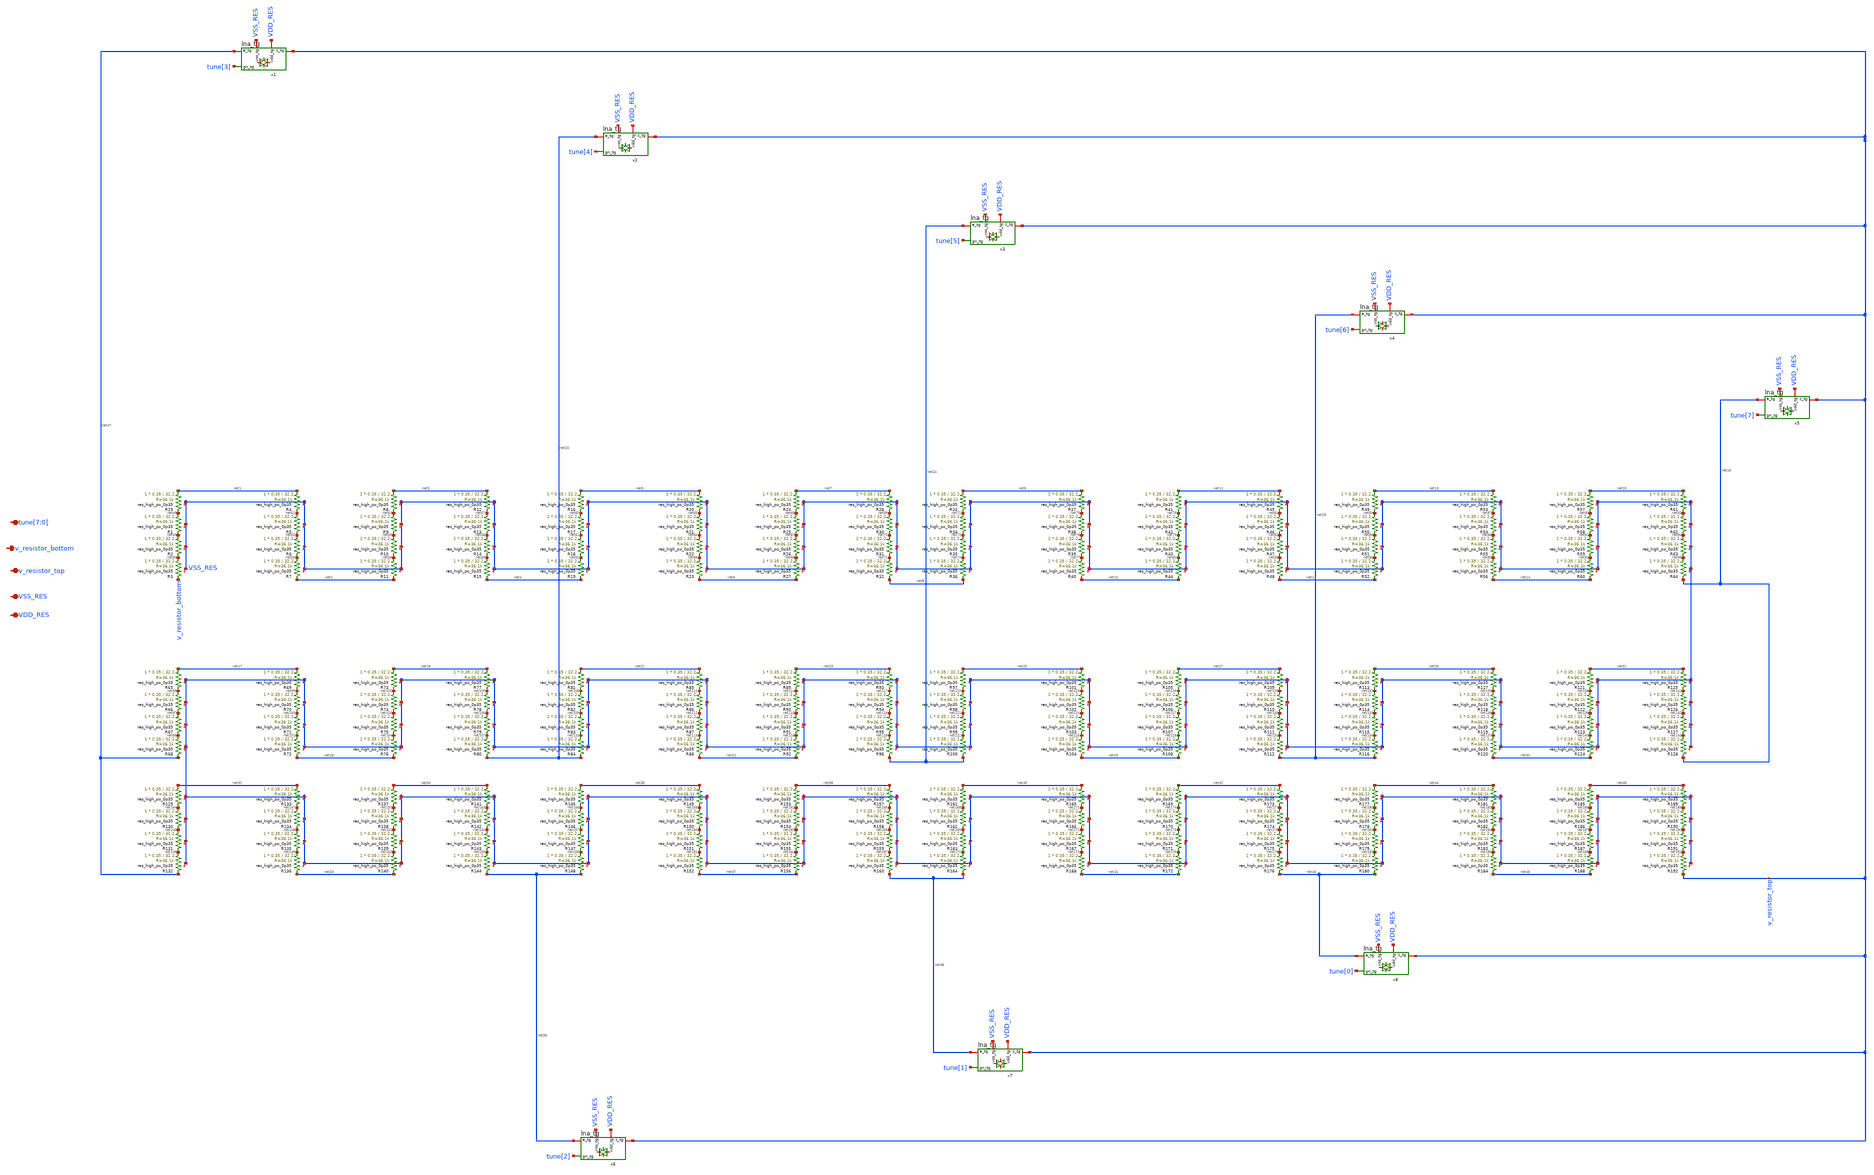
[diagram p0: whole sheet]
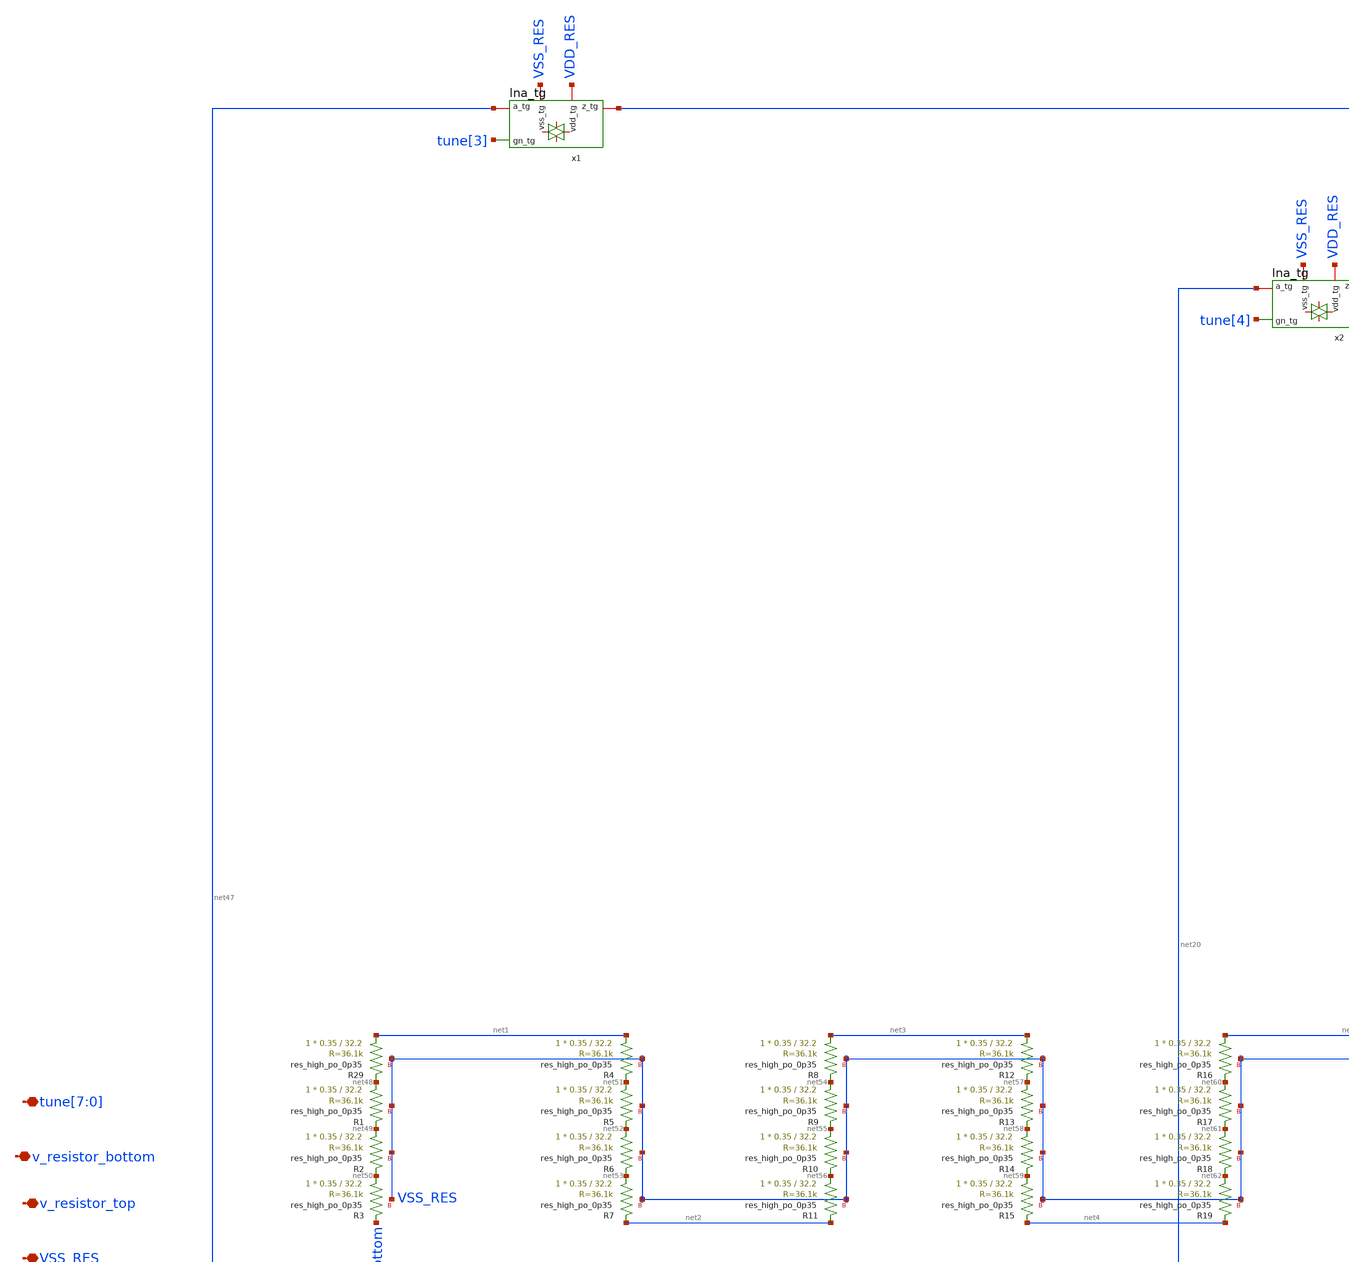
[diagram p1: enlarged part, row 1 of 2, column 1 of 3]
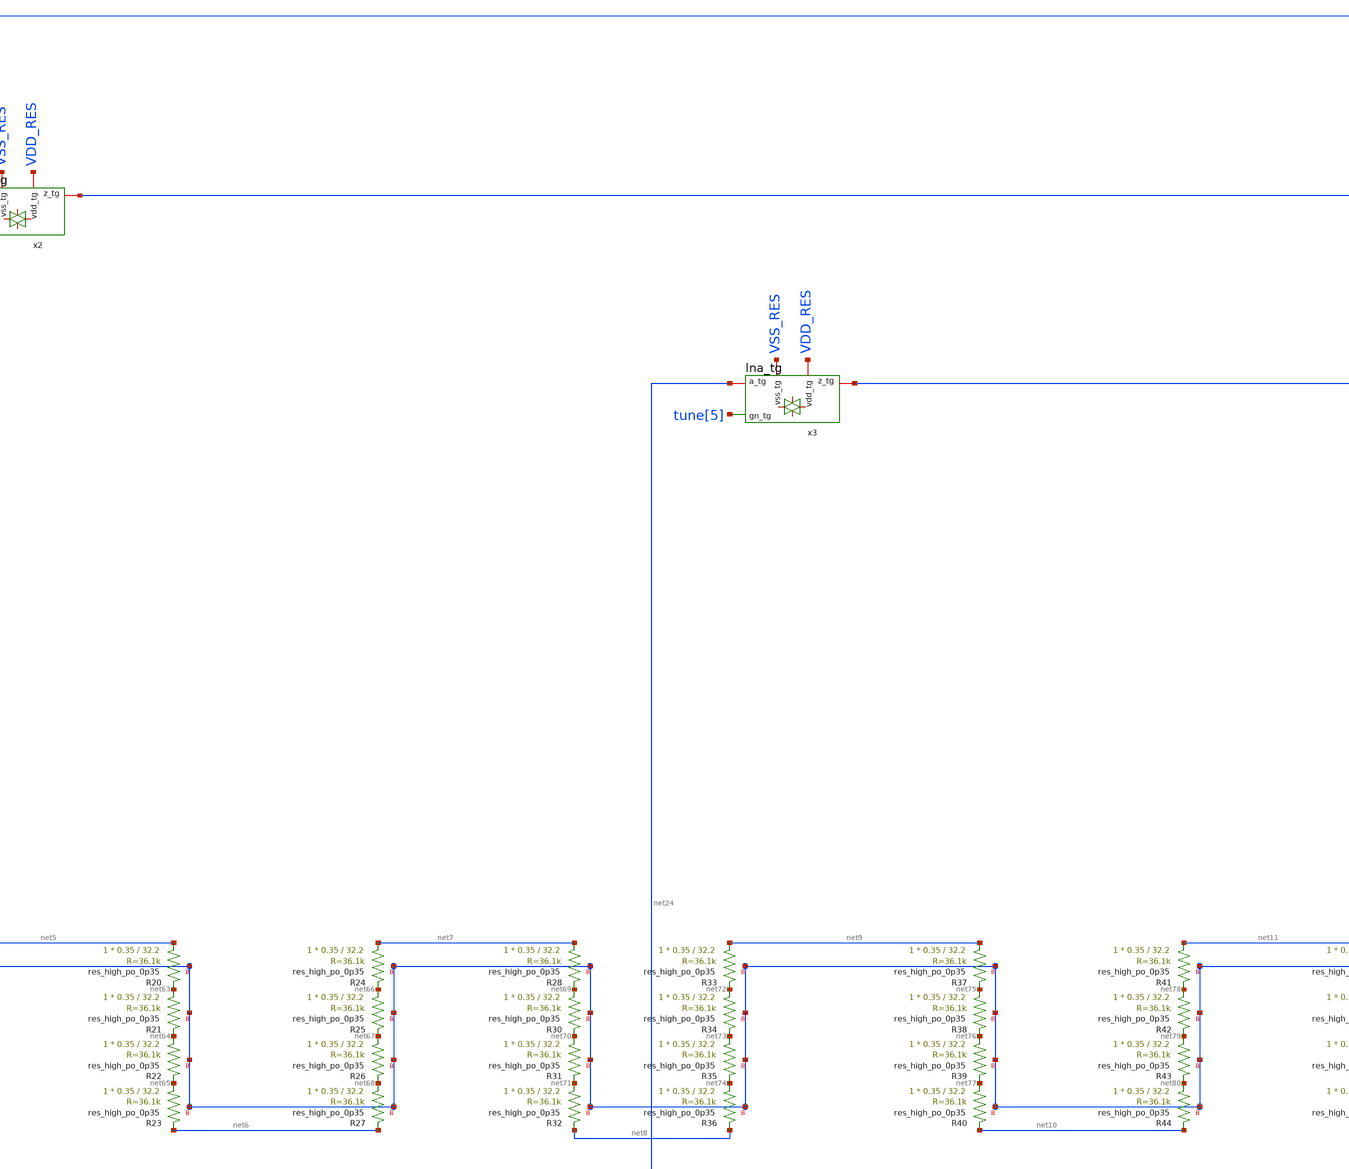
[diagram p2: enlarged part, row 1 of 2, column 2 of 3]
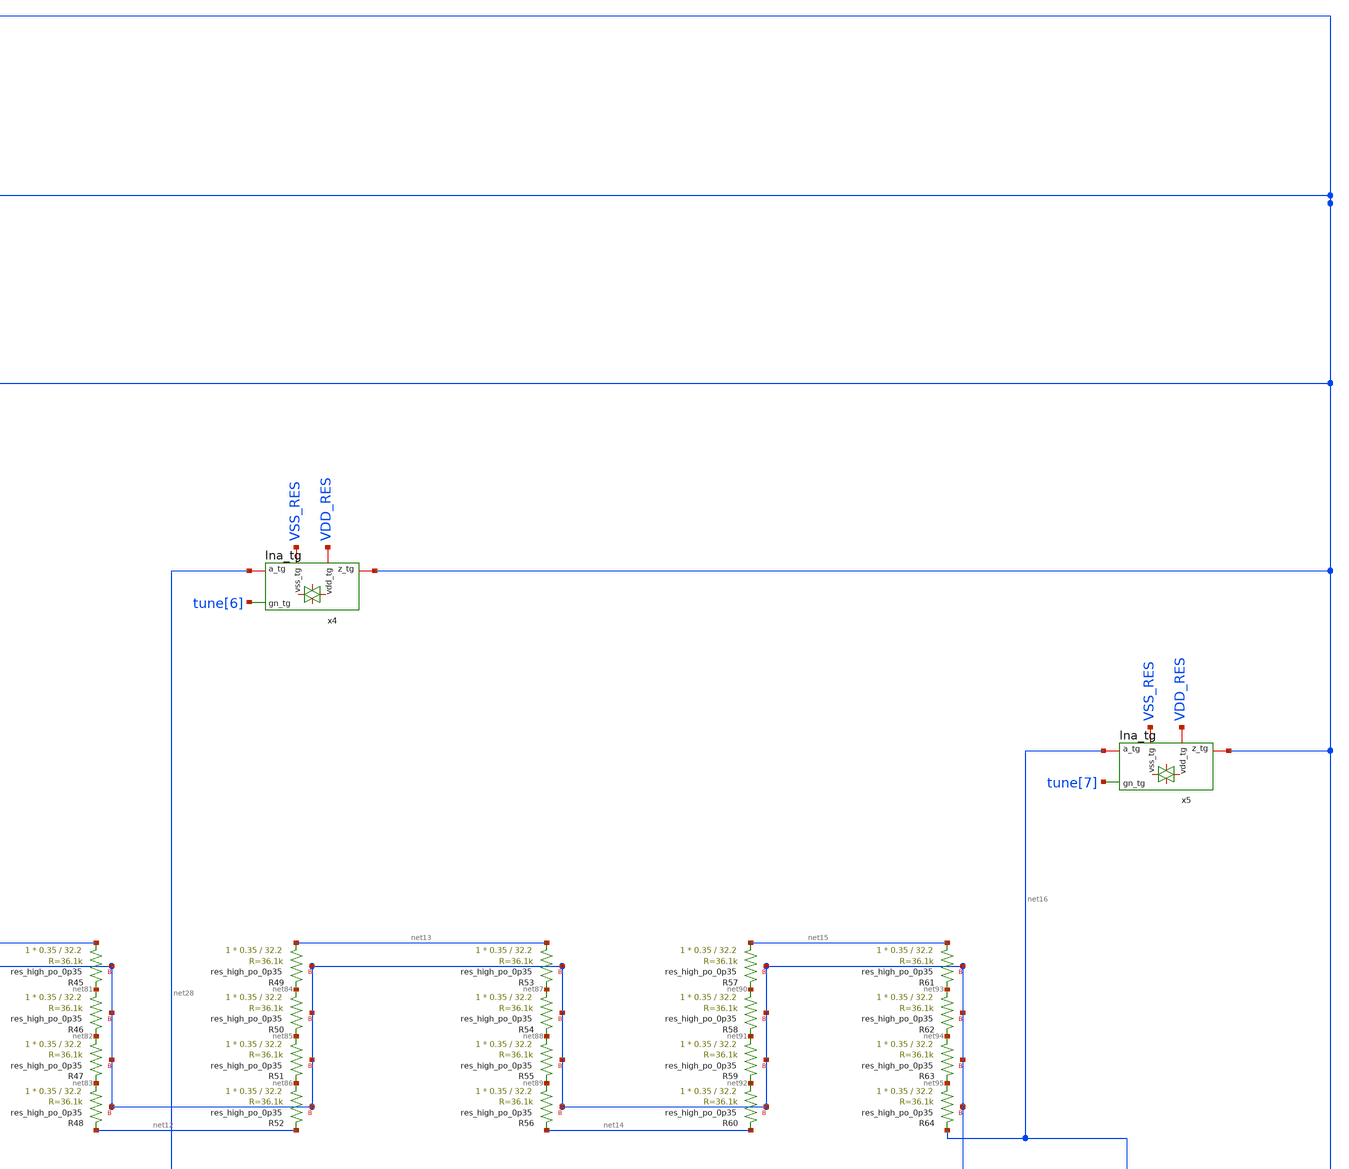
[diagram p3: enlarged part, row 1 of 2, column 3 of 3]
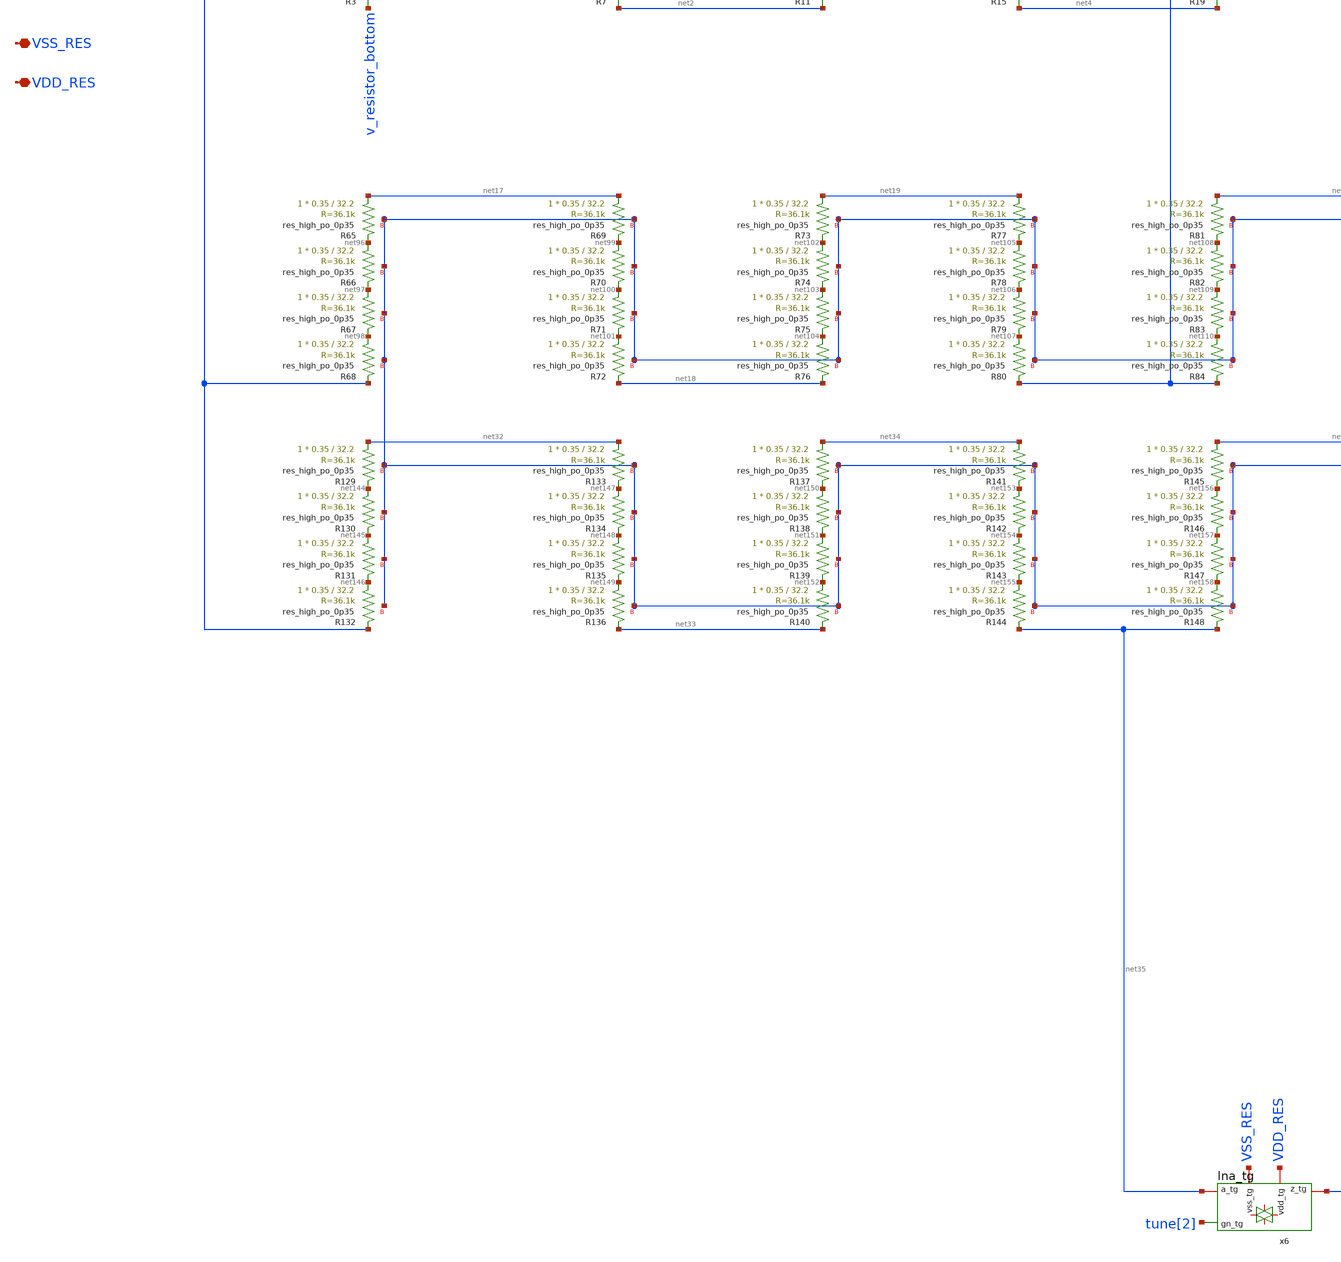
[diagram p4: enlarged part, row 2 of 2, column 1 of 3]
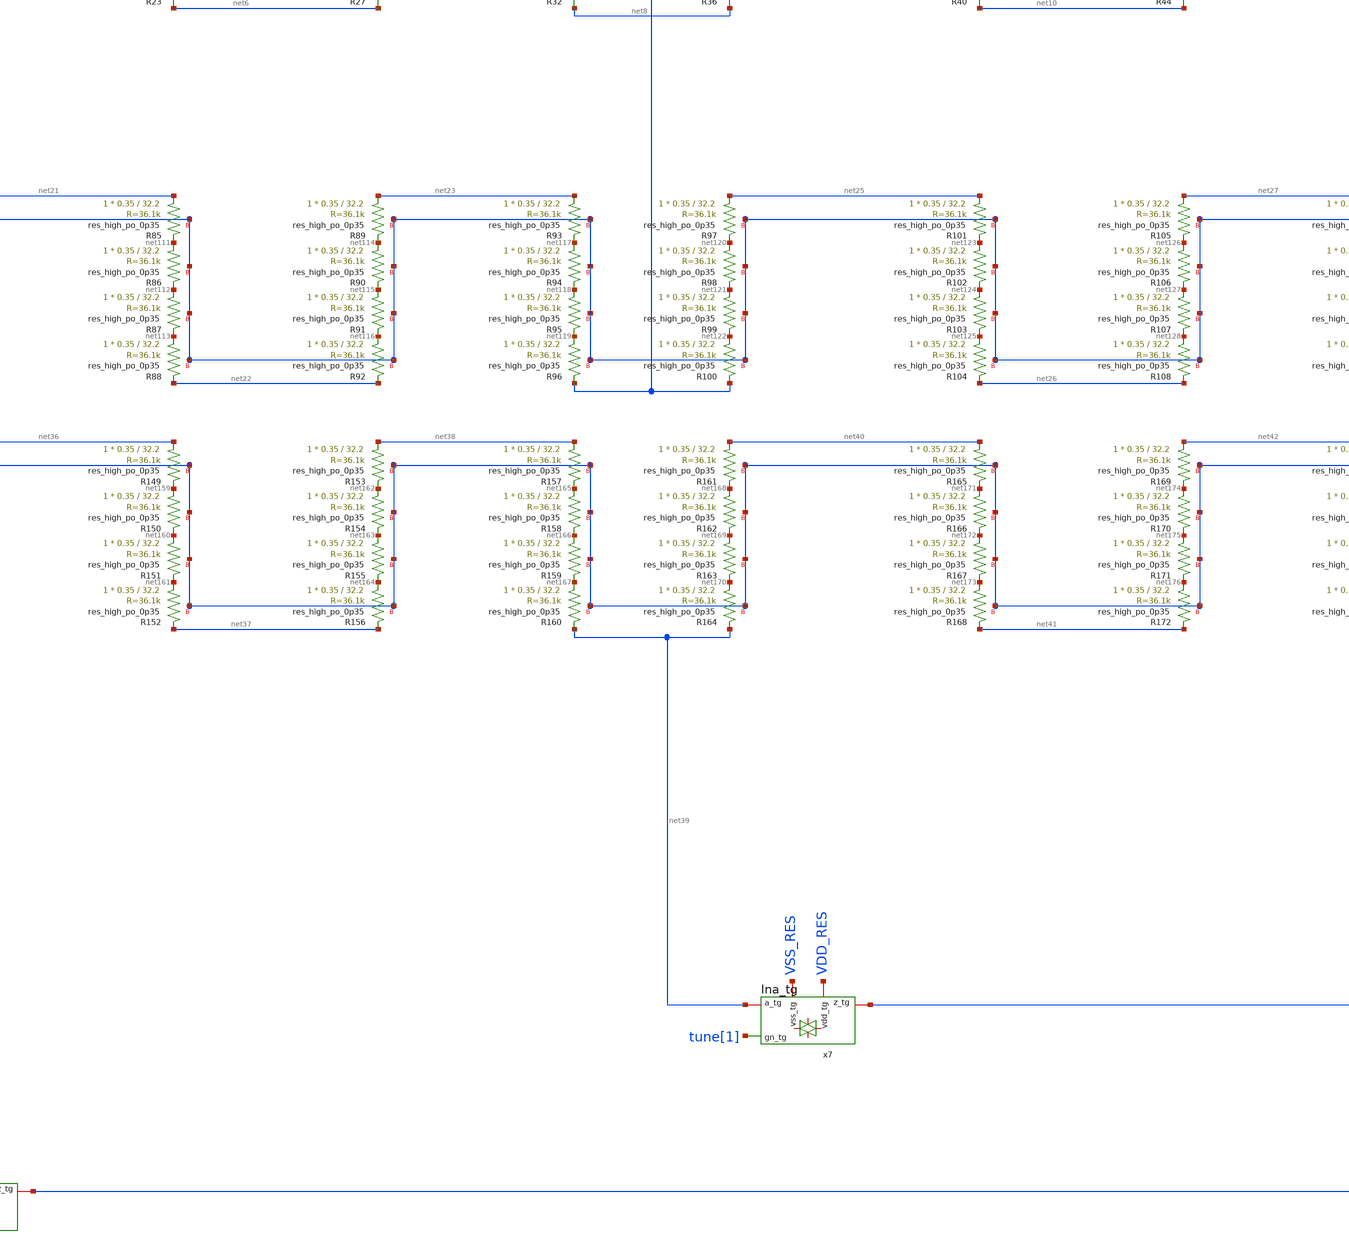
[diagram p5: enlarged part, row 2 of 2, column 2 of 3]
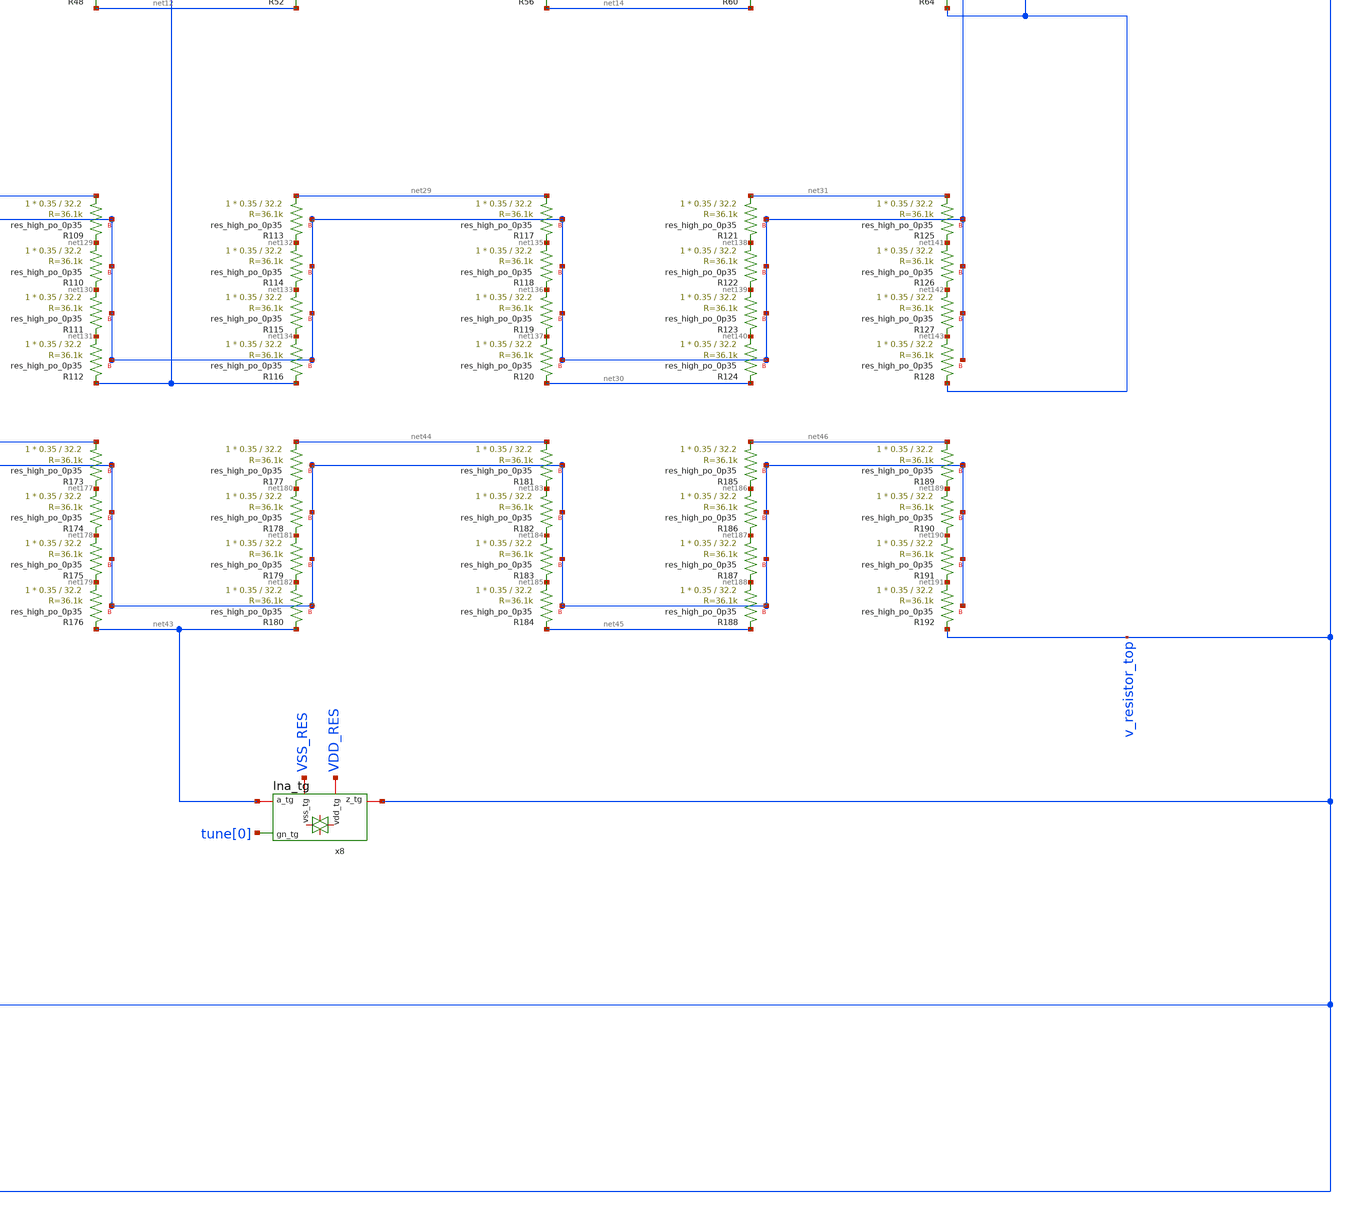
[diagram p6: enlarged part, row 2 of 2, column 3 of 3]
** sch_path: lna_bias_res.sch
**.subckt lna_bias_res v_resistor_bottom v_resistor_top VSS_RES VDD_RES
*+ tune[7],tune[6],tune[5],tune[4],tune[3],tune[2],tune[1],tune[0]
*.iopin v_resistor_bottom
*.iopin v_resistor_top
*.iopin VSS_RES
*.iopin VDD_RES
*.iopin tune[7],tune[6],tune[5],tune[4],tune[3],tune[2],tune[1],tune[0]
XR29 net1 net48 VSS_RES sky130_fd_pr__res_high_po_0p35 L=32.2 mult=1 m=1
XR1 net48 net49 VSS_RES sky130_fd_pr__res_high_po_0p35 L=32.2 mult=1 m=1
XR2 net49 net50 VSS_RES sky130_fd_pr__res_high_po_0p35 L=32.2 mult=1 m=1
XR3 net50 v_resistor_bottom VSS_RES sky130_fd_pr__res_high_po_0p35 L=32.2 mult=1 m=1
XR4 net1 net51 VSS_RES sky130_fd_pr__res_high_po_0p35 L=32.2 mult=1 m=1
XR5 net51 net52 VSS_RES sky130_fd_pr__res_high_po_0p35 L=32.2 mult=1 m=1
XR6 net52 net53 VSS_RES sky130_fd_pr__res_high_po_0p35 L=32.2 mult=1 m=1
XR7 net53 net2 VSS_RES sky130_fd_pr__res_high_po_0p35 L=32.2 mult=1 m=1
XR8 net3 net54 VSS_RES sky130_fd_pr__res_high_po_0p35 L=32.2 mult=1 m=1
XR9 net54 net55 VSS_RES sky130_fd_pr__res_high_po_0p35 L=32.2 mult=1 m=1
XR10 net55 net56 VSS_RES sky130_fd_pr__res_high_po_0p35 L=32.2 mult=1 m=1
XR11 net56 net2 VSS_RES sky130_fd_pr__res_high_po_0p35 L=32.2 mult=1 m=1
XR12 net3 net57 VSS_RES sky130_fd_pr__res_high_po_0p35 L=32.2 mult=1 m=1
XR13 net57 net58 VSS_RES sky130_fd_pr__res_high_po_0p35 L=32.2 mult=1 m=1
XR14 net58 net59 VSS_RES sky130_fd_pr__res_high_po_0p35 L=32.2 mult=1 m=1
XR15 net59 net4 VSS_RES sky130_fd_pr__res_high_po_0p35 L=32.2 mult=1 m=1
XR16 net5 net60 VSS_RES sky130_fd_pr__res_high_po_0p35 L=32.2 mult=1 m=1
XR17 net60 net61 VSS_RES sky130_fd_pr__res_high_po_0p35 L=32.2 mult=1 m=1
XR18 net61 net62 VSS_RES sky130_fd_pr__res_high_po_0p35 L=32.2 mult=1 m=1
XR19 net62 net4 VSS_RES sky130_fd_pr__res_high_po_0p35 L=32.2 mult=1 m=1
XR20 net5 net63 VSS_RES sky130_fd_pr__res_high_po_0p35 L=32.2 mult=1 m=1
XR21 net63 net64 VSS_RES sky130_fd_pr__res_high_po_0p35 L=32.2 mult=1 m=1
XR22 net64 net65 VSS_RES sky130_fd_pr__res_high_po_0p35 L=32.2 mult=1 m=1
XR23 net65 net6 VSS_RES sky130_fd_pr__res_high_po_0p35 L=32.2 mult=1 m=1
XR24 net7 net66 VSS_RES sky130_fd_pr__res_high_po_0p35 L=32.2 mult=1 m=1
XR25 net66 net67 VSS_RES sky130_fd_pr__res_high_po_0p35 L=32.2 mult=1 m=1
XR26 net67 net68 VSS_RES sky130_fd_pr__res_high_po_0p35 L=32.2 mult=1 m=1
XR27 net68 net6 VSS_RES sky130_fd_pr__res_high_po_0p35 L=32.2 mult=1 m=1
XR28 net7 net69 VSS_RES sky130_fd_pr__res_high_po_0p35 L=32.2 mult=1 m=1
XR30 net69 net70 VSS_RES sky130_fd_pr__res_high_po_0p35 L=32.2 mult=1 m=1
XR31 net70 net71 VSS_RES sky130_fd_pr__res_high_po_0p35 L=32.2 mult=1 m=1
XR32 net71 net8 VSS_RES sky130_fd_pr__res_high_po_0p35 L=32.2 mult=1 m=1
XR33 net9 net72 VSS_RES sky130_fd_pr__res_high_po_0p35 L=32.2 mult=1 m=1
XR34 net72 net73 VSS_RES sky130_fd_pr__res_high_po_0p35 L=32.2 mult=1 m=1
XR35 net73 net74 VSS_RES sky130_fd_pr__res_high_po_0p35 L=32.2 mult=1 m=1
XR36 net74 net8 VSS_RES sky130_fd_pr__res_high_po_0p35 L=32.2 mult=1 m=1
XR37 net9 net75 VSS_RES sky130_fd_pr__res_high_po_0p35 L=32.2 mult=1 m=1
XR38 net75 net76 VSS_RES sky130_fd_pr__res_high_po_0p35 L=32.2 mult=1 m=1
XR39 net76 net77 VSS_RES sky130_fd_pr__res_high_po_0p35 L=32.2 mult=1 m=1
XR40 net77 net10 VSS_RES sky130_fd_pr__res_high_po_0p35 L=32.2 mult=1 m=1
XR41 net11 net78 VSS_RES sky130_fd_pr__res_high_po_0p35 L=32.2 mult=1 m=1
XR42 net78 net79 VSS_RES sky130_fd_pr__res_high_po_0p35 L=32.2 mult=1 m=1
XR43 net79 net80 VSS_RES sky130_fd_pr__res_high_po_0p35 L=32.2 mult=1 m=1
XR44 net80 net10 VSS_RES sky130_fd_pr__res_high_po_0p35 L=32.2 mult=1 m=1
XR45 net11 net81 VSS_RES sky130_fd_pr__res_high_po_0p35 L=32.2 mult=1 m=1
XR46 net81 net82 VSS_RES sky130_fd_pr__res_high_po_0p35 L=32.2 mult=1 m=1
XR47 net82 net83 VSS_RES sky130_fd_pr__res_high_po_0p35 L=32.2 mult=1 m=1
XR48 net83 net12 VSS_RES sky130_fd_pr__res_high_po_0p35 L=32.2 mult=1 m=1
XR49 net13 net84 VSS_RES sky130_fd_pr__res_high_po_0p35 L=32.2 mult=1 m=1
XR50 net84 net85 VSS_RES sky130_fd_pr__res_high_po_0p35 L=32.2 mult=1 m=1
XR51 net85 net86 VSS_RES sky130_fd_pr__res_high_po_0p35 L=32.2 mult=1 m=1
XR52 net86 net12 VSS_RES sky130_fd_pr__res_high_po_0p35 L=32.2 mult=1 m=1
XR53 net13 net87 VSS_RES sky130_fd_pr__res_high_po_0p35 L=32.2 mult=1 m=1
XR54 net87 net88 VSS_RES sky130_fd_pr__res_high_po_0p35 L=32.2 mult=1 m=1
XR55 net88 net89 VSS_RES sky130_fd_pr__res_high_po_0p35 L=32.2 mult=1 m=1
XR56 net89 net14 VSS_RES sky130_fd_pr__res_high_po_0p35 L=32.2 mult=1 m=1
XR57 net15 net90 VSS_RES sky130_fd_pr__res_high_po_0p35 L=32.2 mult=1 m=1
XR58 net90 net91 VSS_RES sky130_fd_pr__res_high_po_0p35 L=32.2 mult=1 m=1
XR59 net91 net92 VSS_RES sky130_fd_pr__res_high_po_0p35 L=32.2 mult=1 m=1
XR60 net92 net14 VSS_RES sky130_fd_pr__res_high_po_0p35 L=32.2 mult=1 m=1
XR61 net15 net93 VSS_RES sky130_fd_pr__res_high_po_0p35 L=32.2 mult=1 m=1
XR62 net93 net94 VSS_RES sky130_fd_pr__res_high_po_0p35 L=32.2 mult=1 m=1
XR63 net94 net95 VSS_RES sky130_fd_pr__res_high_po_0p35 L=32.2 mult=1 m=1
XR64 net95 net16 VSS_RES sky130_fd_pr__res_high_po_0p35 L=32.2 mult=1 m=1
XR65 net17 net96 VSS_RES sky130_fd_pr__res_high_po_0p35 L=32.2 mult=1 m=1
XR66 net96 net97 VSS_RES sky130_fd_pr__res_high_po_0p35 L=32.2 mult=1 m=1
XR67 net97 net98 VSS_RES sky130_fd_pr__res_high_po_0p35 L=32.2 mult=1 m=1
XR68 net98 net47 VSS_RES sky130_fd_pr__res_high_po_0p35 L=32.2 mult=1 m=1
XR69 net17 net99 VSS_RES sky130_fd_pr__res_high_po_0p35 L=32.2 mult=1 m=1
XR70 net99 net100 VSS_RES sky130_fd_pr__res_high_po_0p35 L=32.2 mult=1 m=1
XR71 net100 net101 VSS_RES sky130_fd_pr__res_high_po_0p35 L=32.2 mult=1 m=1
XR72 net101 net18 VSS_RES sky130_fd_pr__res_high_po_0p35 L=32.2 mult=1 m=1
XR73 net19 net102 VSS_RES sky130_fd_pr__res_high_po_0p35 L=32.2 mult=1 m=1
XR74 net102 net103 VSS_RES sky130_fd_pr__res_high_po_0p35 L=32.2 mult=1 m=1
XR75 net103 net104 VSS_RES sky130_fd_pr__res_high_po_0p35 L=32.2 mult=1 m=1
XR76 net104 net18 VSS_RES sky130_fd_pr__res_high_po_0p35 L=32.2 mult=1 m=1
XR77 net19 net105 VSS_RES sky130_fd_pr__res_high_po_0p35 L=32.2 mult=1 m=1
XR78 net105 net106 VSS_RES sky130_fd_pr__res_high_po_0p35 L=32.2 mult=1 m=1
XR79 net106 net107 VSS_RES sky130_fd_pr__res_high_po_0p35 L=32.2 mult=1 m=1
XR80 net107 net20 VSS_RES sky130_fd_pr__res_high_po_0p35 L=32.2 mult=1 m=1
XR81 net21 net108 VSS_RES sky130_fd_pr__res_high_po_0p35 L=32.2 mult=1 m=1
XR82 net108 net109 VSS_RES sky130_fd_pr__res_high_po_0p35 L=32.2 mult=1 m=1
XR83 net109 net110 VSS_RES sky130_fd_pr__res_high_po_0p35 L=32.2 mult=1 m=1
XR84 net110 net20 VSS_RES sky130_fd_pr__res_high_po_0p35 L=32.2 mult=1 m=1
XR85 net21 net111 VSS_RES sky130_fd_pr__res_high_po_0p35 L=32.2 mult=1 m=1
XR86 net111 net112 VSS_RES sky130_fd_pr__res_high_po_0p35 L=32.2 mult=1 m=1
XR87 net112 net113 VSS_RES sky130_fd_pr__res_high_po_0p35 L=32.2 mult=1 m=1
XR88 net113 net22 VSS_RES sky130_fd_pr__res_high_po_0p35 L=32.2 mult=1 m=1
XR89 net23 net114 VSS_RES sky130_fd_pr__res_high_po_0p35 L=32.2 mult=1 m=1
XR90 net114 net115 VSS_RES sky130_fd_pr__res_high_po_0p35 L=32.2 mult=1 m=1
XR91 net115 net116 VSS_RES sky130_fd_pr__res_high_po_0p35 L=32.2 mult=1 m=1
XR92 net116 net22 VSS_RES sky130_fd_pr__res_high_po_0p35 L=32.2 mult=1 m=1
XR93 net23 net117 VSS_RES sky130_fd_pr__res_high_po_0p35 L=32.2 mult=1 m=1
XR94 net117 net118 VSS_RES sky130_fd_pr__res_high_po_0p35 L=32.2 mult=1 m=1
XR95 net118 net119 VSS_RES sky130_fd_pr__res_high_po_0p35 L=32.2 mult=1 m=1
XR96 net119 net24 VSS_RES sky130_fd_pr__res_high_po_0p35 L=32.2 mult=1 m=1
XR97 net25 net120 VSS_RES sky130_fd_pr__res_high_po_0p35 L=32.2 mult=1 m=1
XR98 net120 net121 VSS_RES sky130_fd_pr__res_high_po_0p35 L=32.2 mult=1 m=1
XR99 net121 net122 VSS_RES sky130_fd_pr__res_high_po_0p35 L=32.2 mult=1 m=1
XR100 net122 net24 VSS_RES sky130_fd_pr__res_high_po_0p35 L=32.2 mult=1 m=1
XR101 net25 net123 VSS_RES sky130_fd_pr__res_high_po_0p35 L=32.2 mult=1 m=1
XR102 net123 net124 VSS_RES sky130_fd_pr__res_high_po_0p35 L=32.2 mult=1 m=1
XR103 net124 net125 VSS_RES sky130_fd_pr__res_high_po_0p35 L=32.2 mult=1 m=1
XR104 net125 net26 VSS_RES sky130_fd_pr__res_high_po_0p35 L=32.2 mult=1 m=1
XR105 net27 net126 VSS_RES sky130_fd_pr__res_high_po_0p35 L=32.2 mult=1 m=1
XR106 net126 net127 VSS_RES sky130_fd_pr__res_high_po_0p35 L=32.2 mult=1 m=1
XR107 net127 net128 VSS_RES sky130_fd_pr__res_high_po_0p35 L=32.2 mult=1 m=1
XR108 net128 net26 VSS_RES sky130_fd_pr__res_high_po_0p35 L=32.2 mult=1 m=1
XR109 net27 net129 VSS_RES sky130_fd_pr__res_high_po_0p35 L=32.2 mult=1 m=1
XR110 net129 net130 VSS_RES sky130_fd_pr__res_high_po_0p35 L=32.2 mult=1 m=1
XR111 net130 net131 VSS_RES sky130_fd_pr__res_high_po_0p35 L=32.2 mult=1 m=1
XR112 net131 net28 VSS_RES sky130_fd_pr__res_high_po_0p35 L=32.2 mult=1 m=1
XR113 net29 net132 VSS_RES sky130_fd_pr__res_high_po_0p35 L=32.2 mult=1 m=1
XR114 net132 net133 VSS_RES sky130_fd_pr__res_high_po_0p35 L=32.2 mult=1 m=1
XR115 net133 net134 VSS_RES sky130_fd_pr__res_high_po_0p35 L=32.2 mult=1 m=1
XR116 net134 net28 VSS_RES sky130_fd_pr__res_high_po_0p35 L=32.2 mult=1 m=1
XR117 net29 net135 VSS_RES sky130_fd_pr__res_high_po_0p35 L=32.2 mult=1 m=1
XR118 net135 net136 VSS_RES sky130_fd_pr__res_high_po_0p35 L=32.2 mult=1 m=1
XR119 net136 net137 VSS_RES sky130_fd_pr__res_high_po_0p35 L=32.2 mult=1 m=1
XR120 net137 net30 VSS_RES sky130_fd_pr__res_high_po_0p35 L=32.2 mult=1 m=1
XR121 net31 net138 VSS_RES sky130_fd_pr__res_high_po_0p35 L=32.2 mult=1 m=1
XR122 net138 net139 VSS_RES sky130_fd_pr__res_high_po_0p35 L=32.2 mult=1 m=1
XR123 net139 net140 VSS_RES sky130_fd_pr__res_high_po_0p35 L=32.2 mult=1 m=1
XR124 net140 net30 VSS_RES sky130_fd_pr__res_high_po_0p35 L=32.2 mult=1 m=1
XR125 net31 net141 VSS_RES sky130_fd_pr__res_high_po_0p35 L=32.2 mult=1 m=1
XR126 net141 net142 VSS_RES sky130_fd_pr__res_high_po_0p35 L=32.2 mult=1 m=1
XR127 net142 net143 VSS_RES sky130_fd_pr__res_high_po_0p35 L=32.2 mult=1 m=1
XR128 net143 net16 VSS_RES sky130_fd_pr__res_high_po_0p35 L=32.2 mult=1 m=1
XR129 net32 net144 VSS_RES sky130_fd_pr__res_high_po_0p35 L=32.2 mult=1 m=1
XR130 net144 net145 VSS_RES sky130_fd_pr__res_high_po_0p35 L=32.2 mult=1 m=1
XR131 net145 net146 VSS_RES sky130_fd_pr__res_high_po_0p35 L=32.2 mult=1 m=1
XR132 net146 net47 VSS_RES sky130_fd_pr__res_high_po_0p35 L=32.2 mult=1 m=1
XR133 net32 net147 VSS_RES sky130_fd_pr__res_high_po_0p35 L=32.2 mult=1 m=1
XR134 net147 net148 VSS_RES sky130_fd_pr__res_high_po_0p35 L=32.2 mult=1 m=1
XR135 net148 net149 VSS_RES sky130_fd_pr__res_high_po_0p35 L=32.2 mult=1 m=1
XR136 net149 net33 VSS_RES sky130_fd_pr__res_high_po_0p35 L=32.2 mult=1 m=1
XR137 net34 net150 VSS_RES sky130_fd_pr__res_high_po_0p35 L=32.2 mult=1 m=1
XR138 net150 net151 VSS_RES sky130_fd_pr__res_high_po_0p35 L=32.2 mult=1 m=1
XR139 net151 net152 VSS_RES sky130_fd_pr__res_high_po_0p35 L=32.2 mult=1 m=1
XR140 net152 net33 VSS_RES sky130_fd_pr__res_high_po_0p35 L=32.2 mult=1 m=1
XR141 net34 net153 VSS_RES sky130_fd_pr__res_high_po_0p35 L=32.2 mult=1 m=1
XR142 net153 net154 VSS_RES sky130_fd_pr__res_high_po_0p35 L=32.2 mult=1 m=1
XR143 net154 net155 VSS_RES sky130_fd_pr__res_high_po_0p35 L=32.2 mult=1 m=1
XR144 net155 net35 VSS_RES sky130_fd_pr__res_high_po_0p35 L=32.2 mult=1 m=1
XR145 net36 net156 VSS_RES sky130_fd_pr__res_high_po_0p35 L=32.2 mult=1 m=1
XR146 net156 net157 VSS_RES sky130_fd_pr__res_high_po_0p35 L=32.2 mult=1 m=1
XR147 net157 net158 VSS_RES sky130_fd_pr__res_high_po_0p35 L=32.2 mult=1 m=1
XR148 net158 net35 VSS_RES sky130_fd_pr__res_high_po_0p35 L=32.2 mult=1 m=1
XR149 net36 net159 VSS_RES sky130_fd_pr__res_high_po_0p35 L=32.2 mult=1 m=1
XR150 net159 net160 VSS_RES sky130_fd_pr__res_high_po_0p35 L=32.2 mult=1 m=1
XR151 net160 net161 VSS_RES sky130_fd_pr__res_high_po_0p35 L=32.2 mult=1 m=1
XR152 net161 net37 VSS_RES sky130_fd_pr__res_high_po_0p35 L=32.2 mult=1 m=1
XR153 net38 net162 VSS_RES sky130_fd_pr__res_high_po_0p35 L=32.2 mult=1 m=1
XR154 net162 net163 VSS_RES sky130_fd_pr__res_high_po_0p35 L=32.2 mult=1 m=1
XR155 net163 net164 VSS_RES sky130_fd_pr__res_high_po_0p35 L=32.2 mult=1 m=1
XR156 net164 net37 VSS_RES sky130_fd_pr__res_high_po_0p35 L=32.2 mult=1 m=1
XR157 net38 net165 VSS_RES sky130_fd_pr__res_high_po_0p35 L=32.2 mult=1 m=1
XR158 net165 net166 VSS_RES sky130_fd_pr__res_high_po_0p35 L=32.2 mult=1 m=1
XR159 net166 net167 VSS_RES sky130_fd_pr__res_high_po_0p35 L=32.2 mult=1 m=1
XR160 net167 net39 VSS_RES sky130_fd_pr__res_high_po_0p35 L=32.2 mult=1 m=1
XR161 net40 net168 VSS_RES sky130_fd_pr__res_high_po_0p35 L=32.2 mult=1 m=1
XR162 net168 net169 VSS_RES sky130_fd_pr__res_high_po_0p35 L=32.2 mult=1 m=1
XR163 net169 net170 VSS_RES sky130_fd_pr__res_high_po_0p35 L=32.2 mult=1 m=1
XR164 net170 net39 VSS_RES sky130_fd_pr__res_high_po_0p35 L=32.2 mult=1 m=1
XR165 net40 net171 VSS_RES sky130_fd_pr__res_high_po_0p35 L=32.2 mult=1 m=1
XR166 net171 net172 VSS_RES sky130_fd_pr__res_high_po_0p35 L=32.2 mult=1 m=1
XR167 net172 net173 VSS_RES sky130_fd_pr__res_high_po_0p35 L=32.2 mult=1 m=1
XR168 net173 net41 VSS_RES sky130_fd_pr__res_high_po_0p35 L=32.2 mult=1 m=1
XR169 net42 net174 VSS_RES sky130_fd_pr__res_high_po_0p35 L=32.2 mult=1 m=1
XR170 net174 net175 VSS_RES sky130_fd_pr__res_high_po_0p35 L=32.2 mult=1 m=1
XR171 net175 net176 VSS_RES sky130_fd_pr__res_high_po_0p35 L=32.2 mult=1 m=1
XR172 net176 net41 VSS_RES sky130_fd_pr__res_high_po_0p35 L=32.2 mult=1 m=1
XR173 net42 net177 VSS_RES sky130_fd_pr__res_high_po_0p35 L=32.2 mult=1 m=1
XR174 net177 net178 VSS_RES sky130_fd_pr__res_high_po_0p35 L=32.2 mult=1 m=1
XR175 net178 net179 VSS_RES sky130_fd_pr__res_high_po_0p35 L=32.2 mult=1 m=1
XR176 net179 net43 VSS_RES sky130_fd_pr__res_high_po_0p35 L=32.2 mult=1 m=1
XR177 net44 net180 VSS_RES sky130_fd_pr__res_high_po_0p35 L=32.2 mult=1 m=1
XR178 net180 net181 VSS_RES sky130_fd_pr__res_high_po_0p35 L=32.2 mult=1 m=1
XR179 net181 net182 VSS_RES sky130_fd_pr__res_high_po_0p35 L=32.2 mult=1 m=1
XR180 net182 net43 VSS_RES sky130_fd_pr__res_high_po_0p35 L=32.2 mult=1 m=1
XR181 net44 net183 VSS_RES sky130_fd_pr__res_high_po_0p35 L=32.2 mult=1 m=1
XR182 net183 net184 VSS_RES sky130_fd_pr__res_high_po_0p35 L=32.2 mult=1 m=1
XR183 net184 net185 VSS_RES sky130_fd_pr__res_high_po_0p35 L=32.2 mult=1 m=1
XR184 net185 net45 VSS_RES sky130_fd_pr__res_high_po_0p35 L=32.2 mult=1 m=1
XR185 net46 net186 VSS_RES sky130_fd_pr__res_high_po_0p35 L=32.2 mult=1 m=1
XR186 net186 net187 VSS_RES sky130_fd_pr__res_high_po_0p35 L=32.2 mult=1 m=1
XR187 net187 net188 VSS_RES sky130_fd_pr__res_high_po_0p35 L=32.2 mult=1 m=1
XR188 net188 net45 VSS_RES sky130_fd_pr__res_high_po_0p35 L=32.2 mult=1 m=1
XR189 net46 net189 VSS_RES sky130_fd_pr__res_high_po_0p35 L=32.2 mult=1 m=1
XR190 net189 net190 VSS_RES sky130_fd_pr__res_high_po_0p35 L=32.2 mult=1 m=1
XR191 net190 net191 VSS_RES sky130_fd_pr__res_high_po_0p35 L=32.2 mult=1 m=1
XR192 net191 v_resistor_top VSS_RES sky130_fd_pr__res_high_po_0p35 L=32.2 mult=1 m=1
x1 VDD_RES net47 v_resistor_top VSS_RES tune[3] lna_tg
x2 VDD_RES net20 v_resistor_top VSS_RES tune[4] lna_tg
x3 VDD_RES net24 v_resistor_top VSS_RES tune[5] lna_tg
x4 VDD_RES net28 v_resistor_top VSS_RES tune[6] lna_tg
x5 VDD_RES net16 v_resistor_top VSS_RES tune[7] lna_tg
x6 VDD_RES net35 v_resistor_top VSS_RES tune[2] lna_tg
x7 VDD_RES net39 v_resistor_top VSS_RES tune[1] lna_tg
x8 VDD_RES net43 v_resistor_top VSS_RES tune[0] lna_tg
**.ends
.end
